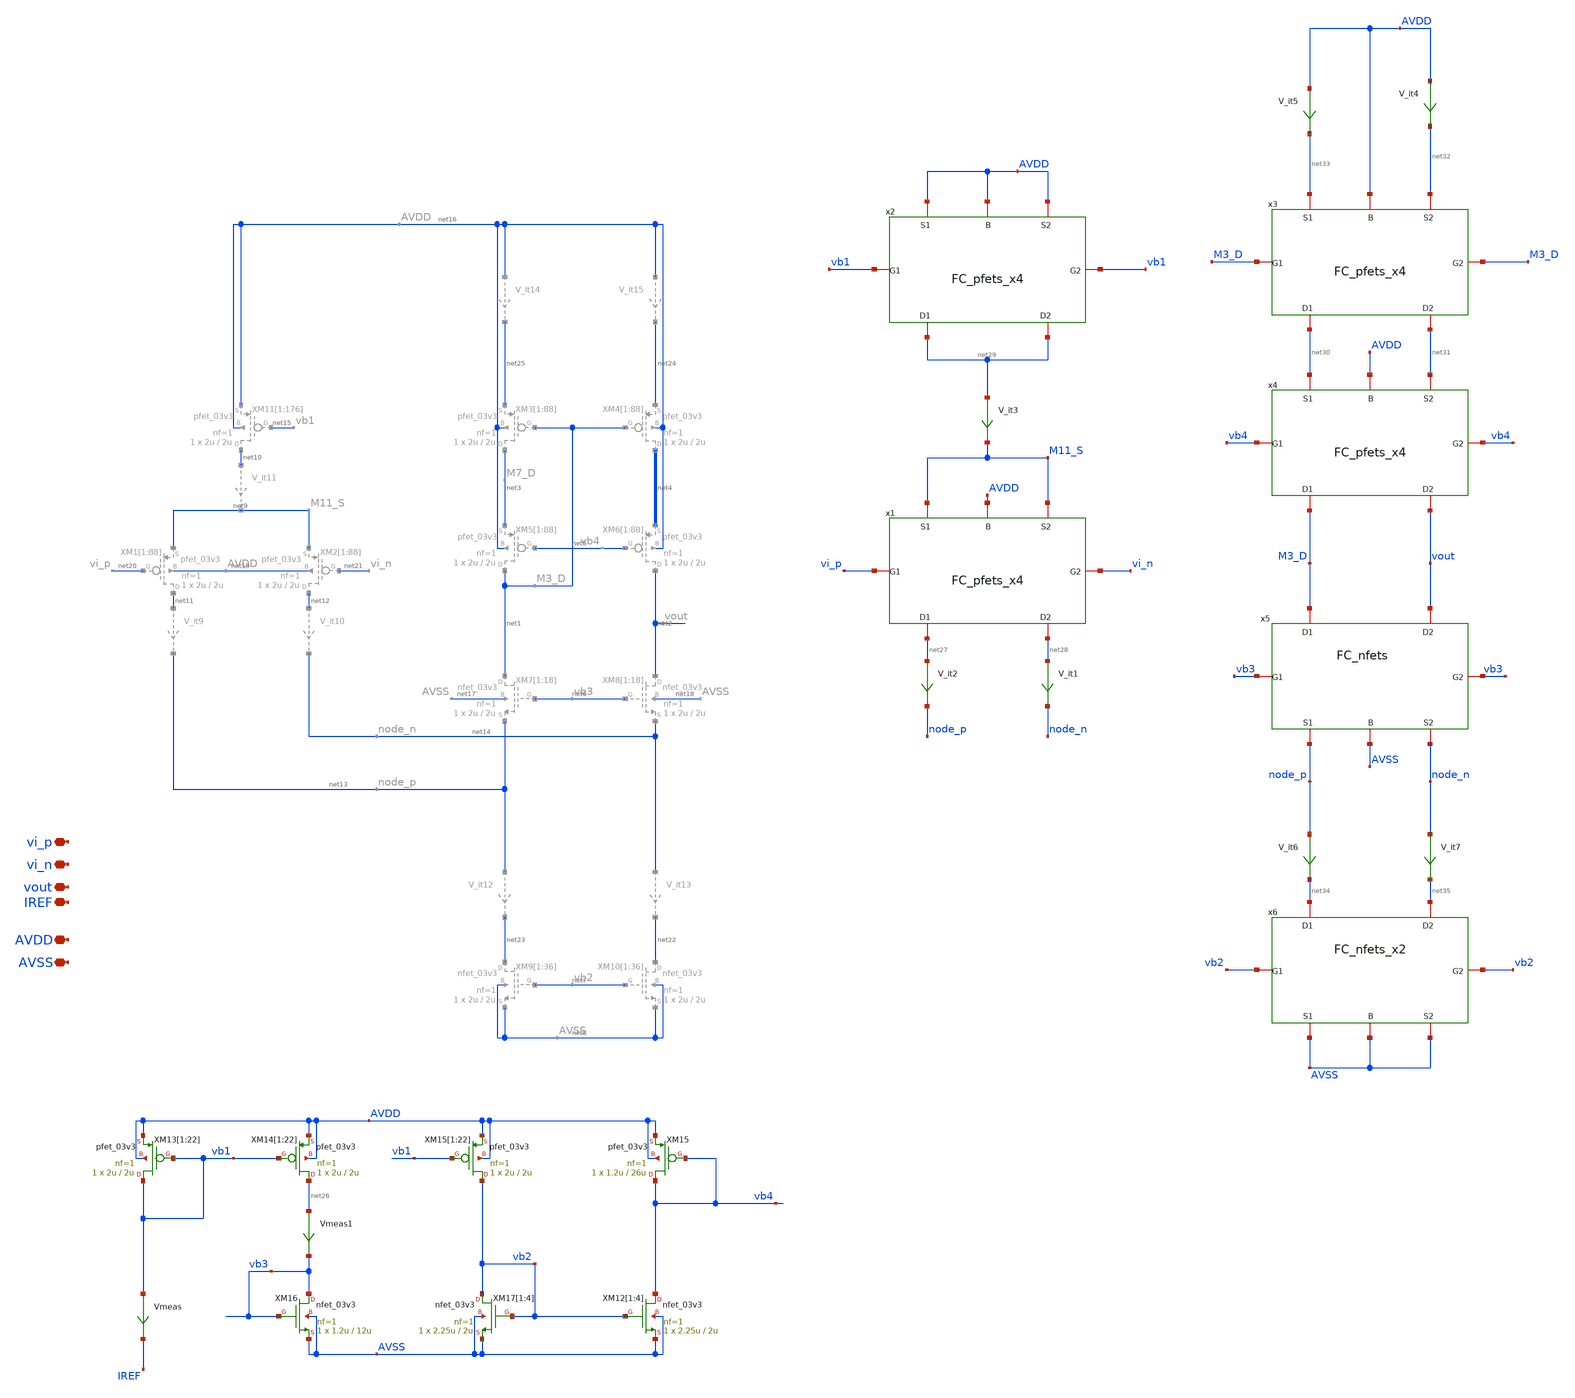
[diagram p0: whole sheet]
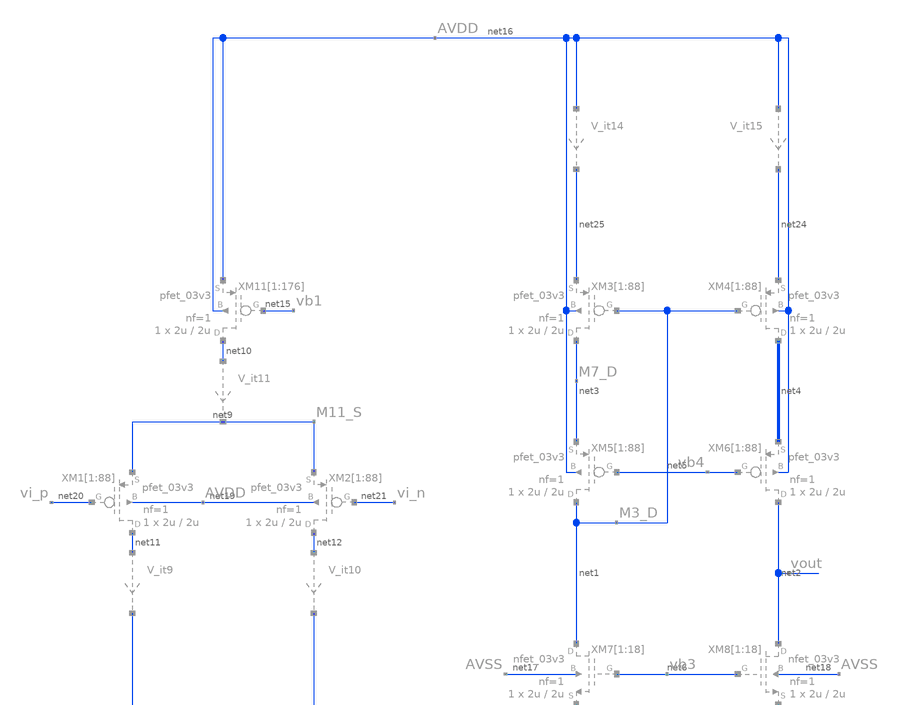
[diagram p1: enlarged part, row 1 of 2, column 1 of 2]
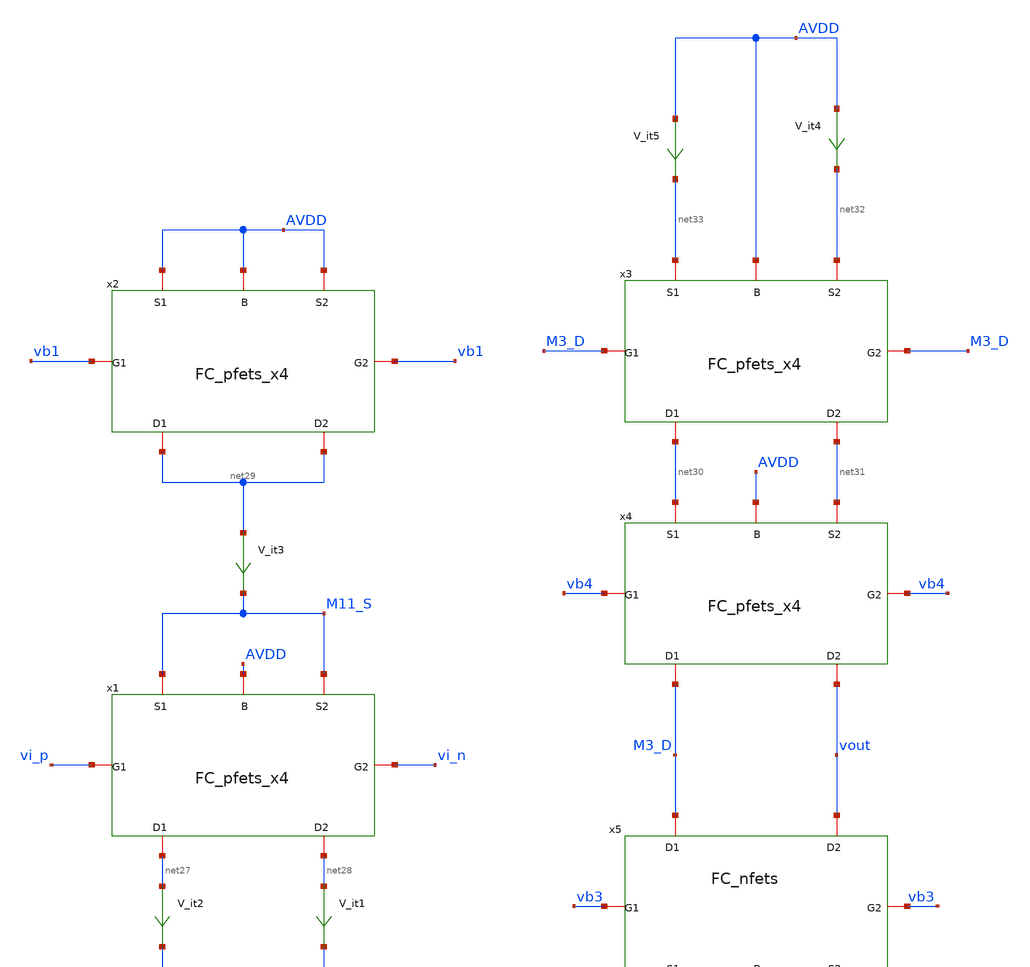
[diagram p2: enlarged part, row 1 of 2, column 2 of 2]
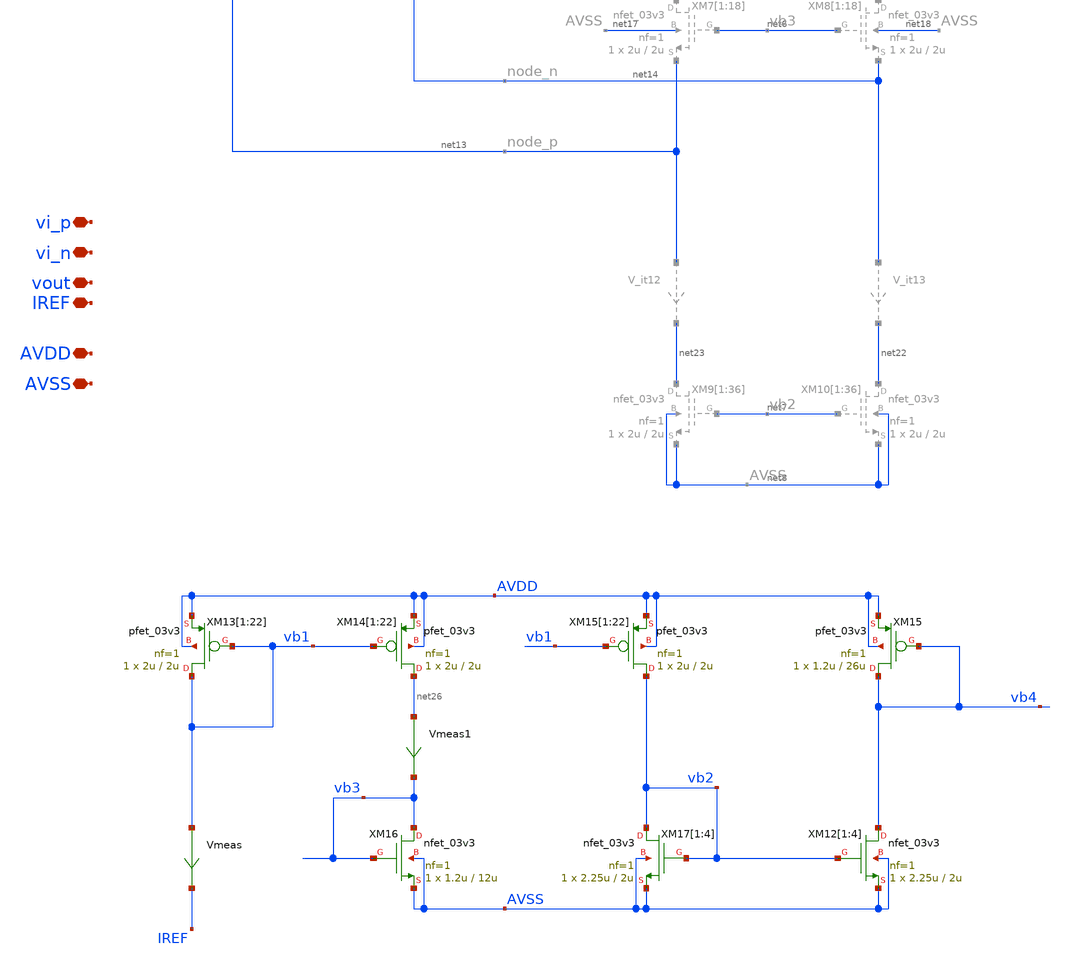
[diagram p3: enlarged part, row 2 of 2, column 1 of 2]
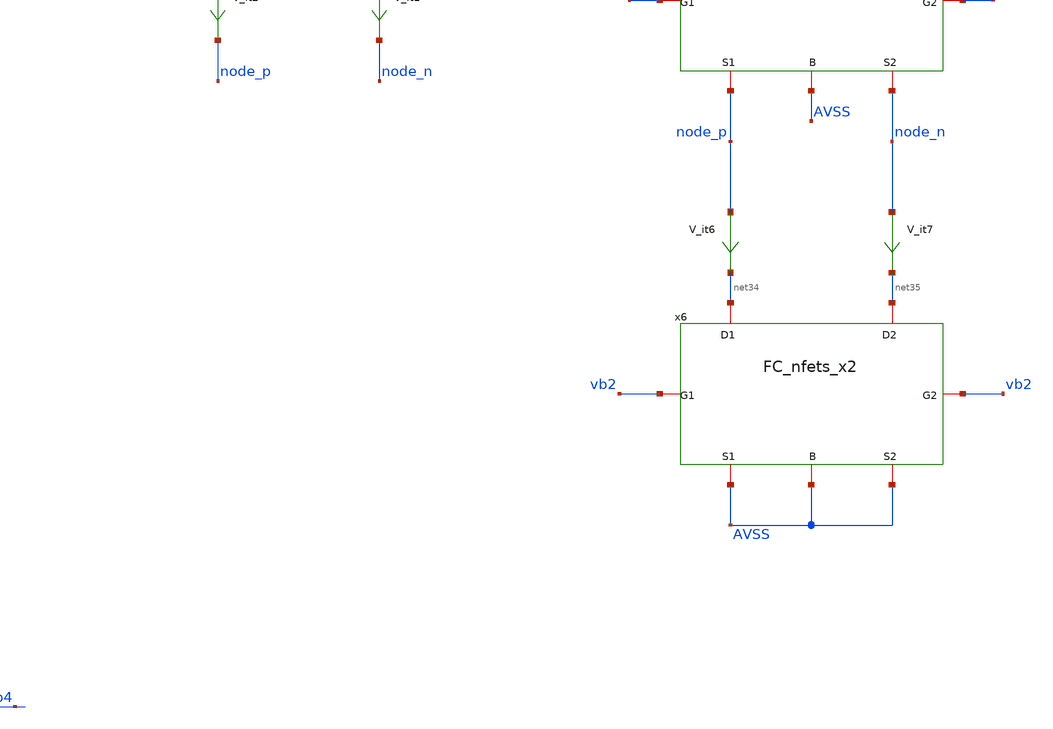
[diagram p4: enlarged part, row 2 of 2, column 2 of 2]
** sch_path: TIA_Filter/Folded/FoldedCascode.sch
**.subckt FoldedCascode AVDD AVSS vout vi_p vi_n IREF
*.iopin AVDD
*.iopin AVSS
*.iopin vout
*.iopin vi_p
*.iopin vi_n
*.iopin IREF
XM16 vb3 vb3 AVSS AVSS nfet_03v3 L=12u W=1.2u nf=1 ad='int((nf+1)/2) * W/nf * 0.18u' as='int((nf+2)/2) * W/nf * 0.18u'
+ pd='2*int((nf+1)/2) * (W/nf + 0.18u)' ps='2*int((nf+2)/2) * (W/nf + 0.18u)' nrd='0.18u / W' nrs='0.18u / W'
+ sa=0 sb=0 sd=0 m=1
XM13[1] vb1 vb1 AVDD AVDD pfet_03v3 L=2u W=2u nf=1 ad='int((nf+1)/2) * W/nf * 0.18u' as='int((nf+2)/2) * W/nf * 0.18u'
+ pd='2*int((nf+1)/2) * (W/nf + 0.18u)' ps='2*int((nf+2)/2) * (W/nf + 0.18u)' nrd='0.18u / W' nrs='0.18u / W'
+ sa=0 sb=0 sd=0 m=1
XM13[2] vb1 vb1 AVDD AVDD pfet_03v3 L=2u W=2u nf=1 ad='int((nf+1)/2) * W/nf * 0.18u' as='int((nf+2)/2) * W/nf * 0.18u'
+ pd='2*int((nf+1)/2) * (W/nf + 0.18u)' ps='2*int((nf+2)/2) * (W/nf + 0.18u)' nrd='0.18u / W' nrs='0.18u / W'
+ sa=0 sb=0 sd=0 m=1
XM13[3] vb1 vb1 AVDD AVDD pfet_03v3 L=2u W=2u nf=1 ad='int((nf+1)/2) * W/nf * 0.18u' as='int((nf+2)/2) * W/nf * 0.18u'
+ pd='2*int((nf+1)/2) * (W/nf + 0.18u)' ps='2*int((nf+2)/2) * (W/nf + 0.18u)' nrd='0.18u / W' nrs='0.18u / W'
+ sa=0 sb=0 sd=0 m=1
XM13[4] vb1 vb1 AVDD AVDD pfet_03v3 L=2u W=2u nf=1 ad='int((nf+1)/2) * W/nf * 0.18u' as='int((nf+2)/2) * W/nf * 0.18u'
+ pd='2*int((nf+1)/2) * (W/nf + 0.18u)' ps='2*int((nf+2)/2) * (W/nf + 0.18u)' nrd='0.18u / W' nrs='0.18u / W'
+ sa=0 sb=0 sd=0 m=1
XM13[5] vb1 vb1 AVDD AVDD pfet_03v3 L=2u W=2u nf=1 ad='int((nf+1)/2) * W/nf * 0.18u' as='int((nf+2)/2) * W/nf * 0.18u'
+ pd='2*int((nf+1)/2) * (W/nf + 0.18u)' ps='2*int((nf+2)/2) * (W/nf + 0.18u)' nrd='0.18u / W' nrs='0.18u / W'
+ sa=0 sb=0 sd=0 m=1
XM13[6] vb1 vb1 AVDD AVDD pfet_03v3 L=2u W=2u nf=1 ad='int((nf+1)/2) * W/nf * 0.18u' as='int((nf+2)/2) * W/nf * 0.18u'
+ pd='2*int((nf+1)/2) * (W/nf + 0.18u)' ps='2*int((nf+2)/2) * (W/nf + 0.18u)' nrd='0.18u / W' nrs='0.18u / W'
+ sa=0 sb=0 sd=0 m=1
XM13[7] vb1 vb1 AVDD AVDD pfet_03v3 L=2u W=2u nf=1 ad='int((nf+1)/2) * W/nf * 0.18u' as='int((nf+2)/2) * W/nf * 0.18u'
+ pd='2*int((nf+1)/2) * (W/nf + 0.18u)' ps='2*int((nf+2)/2) * (W/nf + 0.18u)' nrd='0.18u / W' nrs='0.18u / W'
+ sa=0 sb=0 sd=0 m=1
XM13[8] vb1 vb1 AVDD AVDD pfet_03v3 L=2u W=2u nf=1 ad='int((nf+1)/2) * W/nf * 0.18u' as='int((nf+2)/2) * W/nf * 0.18u'
+ pd='2*int((nf+1)/2) * (W/nf + 0.18u)' ps='2*int((nf+2)/2) * (W/nf + 0.18u)' nrd='0.18u / W' nrs='0.18u / W'
+ sa=0 sb=0 sd=0 m=1
XM13[9] vb1 vb1 AVDD AVDD pfet_03v3 L=2u W=2u nf=1 ad='int((nf+1)/2) * W/nf * 0.18u' as='int((nf+2)/2) * W/nf * 0.18u'
+ pd='2*int((nf+1)/2) * (W/nf + 0.18u)' ps='2*int((nf+2)/2) * (W/nf + 0.18u)' nrd='0.18u / W' nrs='0.18u / W'
+ sa=0 sb=0 sd=0 m=1
XM13[10] vb1 vb1 AVDD AVDD pfet_03v3 L=2u W=2u nf=1 ad='int((nf+1)/2) * W/nf * 0.18u' as='int((nf+2)/2) * W/nf * 0.18u'
+ pd='2*int((nf+1)/2) * (W/nf + 0.18u)' ps='2*int((nf+2)/2) * (W/nf + 0.18u)' nrd='0.18u / W' nrs='0.18u / W'
+ sa=0 sb=0 sd=0 m=1
XM13[11] vb1 vb1 AVDD AVDD pfet_03v3 L=2u W=2u nf=1 ad='int((nf+1)/2) * W/nf * 0.18u' as='int((nf+2)/2) * W/nf * 0.18u'
+ pd='2*int((nf+1)/2) * (W/nf + 0.18u)' ps='2*int((nf+2)/2) * (W/nf + 0.18u)' nrd='0.18u / W' nrs='0.18u / W'
+ sa=0 sb=0 sd=0 m=1
XM13[12] vb1 vb1 AVDD AVDD pfet_03v3 L=2u W=2u nf=1 ad='int((nf+1)/2) * W/nf * 0.18u' as='int((nf+2)/2) * W/nf * 0.18u'
+ pd='2*int((nf+1)/2) * (W/nf + 0.18u)' ps='2*int((nf+2)/2) * (W/nf + 0.18u)' nrd='0.18u / W' nrs='0.18u / W'
+ sa=0 sb=0 sd=0 m=1
XM13[13] vb1 vb1 AVDD AVDD pfet_03v3 L=2u W=2u nf=1 ad='int((nf+1)/2) * W/nf * 0.18u' as='int((nf+2)/2) * W/nf * 0.18u'
+ pd='2*int((nf+1)/2) * (W/nf + 0.18u)' ps='2*int((nf+2)/2) * (W/nf + 0.18u)' nrd='0.18u / W' nrs='0.18u / W'
+ sa=0 sb=0 sd=0 m=1
XM13[14] vb1 vb1 AVDD AVDD pfet_03v3 L=2u W=2u nf=1 ad='int((nf+1)/2) * W/nf * 0.18u' as='int((nf+2)/2) * W/nf * 0.18u'
+ pd='2*int((nf+1)/2) * (W/nf + 0.18u)' ps='2*int((nf+2)/2) * (W/nf + 0.18u)' nrd='0.18u / W' nrs='0.18u / W'
+ sa=0 sb=0 sd=0 m=1
XM13[15] vb1 vb1 AVDD AVDD pfet_03v3 L=2u W=2u nf=1 ad='int((nf+1)/2) * W/nf * 0.18u' as='int((nf+2)/2) * W/nf * 0.18u'
+ pd='2*int((nf+1)/2) * (W/nf + 0.18u)' ps='2*int((nf+2)/2) * (W/nf + 0.18u)' nrd='0.18u / W' nrs='0.18u / W'
+ sa=0 sb=0 sd=0 m=1
XM13[16] vb1 vb1 AVDD AVDD pfet_03v3 L=2u W=2u nf=1 ad='int((nf+1)/2) * W/nf * 0.18u' as='int((nf+2)/2) * W/nf * 0.18u'
+ pd='2*int((nf+1)/2) * (W/nf + 0.18u)' ps='2*int((nf+2)/2) * (W/nf + 0.18u)' nrd='0.18u / W' nrs='0.18u / W'
+ sa=0 sb=0 sd=0 m=1
XM13[17] vb1 vb1 AVDD AVDD pfet_03v3 L=2u W=2u nf=1 ad='int((nf+1)/2) * W/nf * 0.18u' as='int((nf+2)/2) * W/nf * 0.18u'
+ pd='2*int((nf+1)/2) * (W/nf + 0.18u)' ps='2*int((nf+2)/2) * (W/nf + 0.18u)' nrd='0.18u / W' nrs='0.18u / W'
+ sa=0 sb=0 sd=0 m=1
XM13[18] vb1 vb1 AVDD AVDD pfet_03v3 L=2u W=2u nf=1 ad='int((nf+1)/2) * W/nf * 0.18u' as='int((nf+2)/2) * W/nf * 0.18u'
+ pd='2*int((nf+1)/2) * (W/nf + 0.18u)' ps='2*int((nf+2)/2) * (W/nf + 0.18u)' nrd='0.18u / W' nrs='0.18u / W'
+ sa=0 sb=0 sd=0 m=1
XM13[19] vb1 vb1 AVDD AVDD pfet_03v3 L=2u W=2u nf=1 ad='int((nf+1)/2) * W/nf * 0.18u' as='int((nf+2)/2) * W/nf * 0.18u'
+ pd='2*int((nf+1)/2) * (W/nf + 0.18u)' ps='2*int((nf+2)/2) * (W/nf + 0.18u)' nrd='0.18u / W' nrs='0.18u / W'
+ sa=0 sb=0 sd=0 m=1
XM13[20] vb1 vb1 AVDD AVDD pfet_03v3 L=2u W=2u nf=1 ad='int((nf+1)/2) * W/nf * 0.18u' as='int((nf+2)/2) * W/nf * 0.18u'
+ pd='2*int((nf+1)/2) * (W/nf + 0.18u)' ps='2*int((nf+2)/2) * (W/nf + 0.18u)' nrd='0.18u / W' nrs='0.18u / W'
+ sa=0 sb=0 sd=0 m=1
XM13[21] vb1 vb1 AVDD AVDD pfet_03v3 L=2u W=2u nf=1 ad='int((nf+1)/2) * W/nf * 0.18u' as='int((nf+2)/2) * W/nf * 0.18u'
+ pd='2*int((nf+1)/2) * (W/nf + 0.18u)' ps='2*int((nf+2)/2) * (W/nf + 0.18u)' nrd='0.18u / W' nrs='0.18u / W'
+ sa=0 sb=0 sd=0 m=1
XM13[22] vb1 vb1 AVDD AVDD pfet_03v3 L=2u W=2u nf=1 ad='int((nf+1)/2) * W/nf * 0.18u' as='int((nf+2)/2) * W/nf * 0.18u'
+ pd='2*int((nf+1)/2) * (W/nf + 0.18u)' ps='2*int((nf+2)/2) * (W/nf + 0.18u)' nrd='0.18u / W' nrs='0.18u / W'
+ sa=0 sb=0 sd=0 m=1
XM14[1] net26 vb1 AVDD AVDD pfet_03v3 L=2u W=2u nf=1 ad='int((nf+1)/2) * W/nf * 0.18u' as='int((nf+2)/2) * W/nf * 0.18u'
+ pd='2*int((nf+1)/2) * (W/nf + 0.18u)' ps='2*int((nf+2)/2) * (W/nf + 0.18u)' nrd='0.18u / W' nrs='0.18u / W'
+ sa=0 sb=0 sd=0 m=1
XM14[2] net26 vb1 AVDD AVDD pfet_03v3 L=2u W=2u nf=1 ad='int((nf+1)/2) * W/nf * 0.18u' as='int((nf+2)/2) * W/nf * 0.18u'
+ pd='2*int((nf+1)/2) * (W/nf + 0.18u)' ps='2*int((nf+2)/2) * (W/nf + 0.18u)' nrd='0.18u / W' nrs='0.18u / W'
+ sa=0 sb=0 sd=0 m=1
XM14[3] net26 vb1 AVDD AVDD pfet_03v3 L=2u W=2u nf=1 ad='int((nf+1)/2) * W/nf * 0.18u' as='int((nf+2)/2) * W/nf * 0.18u'
+ pd='2*int((nf+1)/2) * (W/nf + 0.18u)' ps='2*int((nf+2)/2) * (W/nf + 0.18u)' nrd='0.18u / W' nrs='0.18u / W'
+ sa=0 sb=0 sd=0 m=1
XM14[4] net26 vb1 AVDD AVDD pfet_03v3 L=2u W=2u nf=1 ad='int((nf+1)/2) * W/nf * 0.18u' as='int((nf+2)/2) * W/nf * 0.18u'
+ pd='2*int((nf+1)/2) * (W/nf + 0.18u)' ps='2*int((nf+2)/2) * (W/nf + 0.18u)' nrd='0.18u / W' nrs='0.18u / W'
+ sa=0 sb=0 sd=0 m=1
XM14[5] net26 vb1 AVDD AVDD pfet_03v3 L=2u W=2u nf=1 ad='int((nf+1)/2) * W/nf * 0.18u' as='int((nf+2)/2) * W/nf * 0.18u'
+ pd='2*int((nf+1)/2) * (W/nf + 0.18u)' ps='2*int((nf+2)/2) * (W/nf + 0.18u)' nrd='0.18u / W' nrs='0.18u / W'
+ sa=0 sb=0 sd=0 m=1
XM14[6] net26 vb1 AVDD AVDD pfet_03v3 L=2u W=2u nf=1 ad='int((nf+1)/2) * W/nf * 0.18u' as='int((nf+2)/2) * W/nf * 0.18u'
+ pd='2*int((nf+1)/2) * (W/nf + 0.18u)' ps='2*int((nf+2)/2) * (W/nf + 0.18u)' nrd='0.18u / W' nrs='0.18u / W'
+ sa=0 sb=0 sd=0 m=1
XM14[7] net26 vb1 AVDD AVDD pfet_03v3 L=2u W=2u nf=1 ad='int((nf+1)/2) * W/nf * 0.18u' as='int((nf+2)/2) * W/nf * 0.18u'
+ pd='2*int((nf+1)/2) * (W/nf + 0.18u)' ps='2*int((nf+2)/2) * (W/nf + 0.18u)' nrd='0.18u / W' nrs='0.18u / W'
+ sa=0 sb=0 sd=0 m=1
XM14[8] net26 vb1 AVDD AVDD pfet_03v3 L=2u W=2u nf=1 ad='int((nf+1)/2) * W/nf * 0.18u' as='int((nf+2)/2) * W/nf * 0.18u'
+ pd='2*int((nf+1)/2) * (W/nf + 0.18u)' ps='2*int((nf+2)/2) * (W/nf + 0.18u)' nrd='0.18u / W' nrs='0.18u / W'
+ sa=0 sb=0 sd=0 m=1
XM14[9] net26 vb1 AVDD AVDD pfet_03v3 L=2u W=2u nf=1 ad='int((nf+1)/2) * W/nf * 0.18u' as='int((nf+2)/2) * W/nf * 0.18u'
+ pd='2*int((nf+1)/2) * (W/nf + 0.18u)' ps='2*int((nf+2)/2) * (W/nf + 0.18u)' nrd='0.18u / W' nrs='0.18u / W'
+ sa=0 sb=0 sd=0 m=1
XM14[10] net26 vb1 AVDD AVDD pfet_03v3 L=2u W=2u nf=1 ad='int((nf+1)/2) * W/nf * 0.18u' as='int((nf+2)/2) * W/nf * 0.18u'
+ pd='2*int((nf+1)/2) * (W/nf + 0.18u)' ps='2*int((nf+2)/2) * (W/nf + 0.18u)' nrd='0.18u / W' nrs='0.18u / W'
+ sa=0 sb=0 sd=0 m=1
XM14[11] net26 vb1 AVDD AVDD pfet_03v3 L=2u W=2u nf=1 ad='int((nf+1)/2) * W/nf * 0.18u' as='int((nf+2)/2) * W/nf * 0.18u'
+ pd='2*int((nf+1)/2) * (W/nf + 0.18u)' ps='2*int((nf+2)/2) * (W/nf + 0.18u)' nrd='0.18u / W' nrs='0.18u / W'
+ sa=0 sb=0 sd=0 m=1
XM14[12] net26 vb1 AVDD AVDD pfet_03v3 L=2u W=2u nf=1 ad='int((nf+1)/2) * W/nf * 0.18u' as='int((nf+2)/2) * W/nf * 0.18u'
+ pd='2*int((nf+1)/2) * (W/nf + 0.18u)' ps='2*int((nf+2)/2) * (W/nf + 0.18u)' nrd='0.18u / W' nrs='0.18u / W'
+ sa=0 sb=0 sd=0 m=1
XM14[13] net26 vb1 AVDD AVDD pfet_03v3 L=2u W=2u nf=1 ad='int((nf+1)/2) * W/nf * 0.18u' as='int((nf+2)/2) * W/nf * 0.18u'
+ pd='2*int((nf+1)/2) * (W/nf + 0.18u)' ps='2*int((nf+2)/2) * (W/nf + 0.18u)' nrd='0.18u / W' nrs='0.18u / W'
+ sa=0 sb=0 sd=0 m=1
XM14[14] net26 vb1 AVDD AVDD pfet_03v3 L=2u W=2u nf=1 ad='int((nf+1)/2) * W/nf * 0.18u' as='int((nf+2)/2) * W/nf * 0.18u'
+ pd='2*int((nf+1)/2) * (W/nf + 0.18u)' ps='2*int((nf+2)/2) * (W/nf + 0.18u)' nrd='0.18u / W' nrs='0.18u / W'
+ sa=0 sb=0 sd=0 m=1
XM14[15] net26 vb1 AVDD AVDD pfet_03v3 L=2u W=2u nf=1 ad='int((nf+1)/2) * W/nf * 0.18u' as='int((nf+2)/2) * W/nf * 0.18u'
+ pd='2*int((nf+1)/2) * (W/nf + 0.18u)' ps='2*int((nf+2)/2) * (W/nf + 0.18u)' nrd='0.18u / W' nrs='0.18u / W'
+ sa=0 sb=0 sd=0 m=1
XM14[16] net26 vb1 AVDD AVDD pfet_03v3 L=2u W=2u nf=1 ad='int((nf+1)/2) * W/nf * 0.18u' as='int((nf+2)/2) * W/nf * 0.18u'
+ pd='2*int((nf+1)/2) * (W/nf + 0.18u)' ps='2*int((nf+2)/2) * (W/nf + 0.18u)' nrd='0.18u / W' nrs='0.18u / W'
+ sa=0 sb=0 sd=0 m=1
XM14[17] net26 vb1 AVDD AVDD pfet_03v3 L=2u W=2u nf=1 ad='int((nf+1)/2) * W/nf * 0.18u' as='int((nf+2)/2) * W/nf * 0.18u'
+ pd='2*int((nf+1)/2) * (W/nf + 0.18u)' ps='2*int((nf+2)/2) * (W/nf + 0.18u)' nrd='0.18u / W' nrs='0.18u / W'
+ sa=0 sb=0 sd=0 m=1
XM14[18] net26 vb1 AVDD AVDD pfet_03v3 L=2u W=2u nf=1 ad='int((nf+1)/2) * W/nf * 0.18u' as='int((nf+2)/2) * W/nf * 0.18u'
+ pd='2*int((nf+1)/2) * (W/nf + 0.18u)' ps='2*int((nf+2)/2) * (W/nf + 0.18u)' nrd='0.18u / W' nrs='0.18u / W'
+ sa=0 sb=0 sd=0 m=1
XM14[19] net26 vb1 AVDD AVDD pfet_03v3 L=2u W=2u nf=1 ad='int((nf+1)/2) * W/nf * 0.18u' as='int((nf+2)/2) * W/nf * 0.18u'
+ pd='2*int((nf+1)/2) * (W/nf + 0.18u)' ps='2*int((nf+2)/2) * (W/nf + 0.18u)' nrd='0.18u / W' nrs='0.18u / W'
+ sa=0 sb=0 sd=0 m=1
XM14[20] net26 vb1 AVDD AVDD pfet_03v3 L=2u W=2u nf=1 ad='int((nf+1)/2) * W/nf * 0.18u' as='int((nf+2)/2) * W/nf * 0.18u'
+ pd='2*int((nf+1)/2) * (W/nf + 0.18u)' ps='2*int((nf+2)/2) * (W/nf + 0.18u)' nrd='0.18u / W' nrs='0.18u / W'
+ sa=0 sb=0 sd=0 m=1
XM14[21] net26 vb1 AVDD AVDD pfet_03v3 L=2u W=2u nf=1 ad='int((nf+1)/2) * W/nf * 0.18u' as='int((nf+2)/2) * W/nf * 0.18u'
+ pd='2*int((nf+1)/2) * (W/nf + 0.18u)' ps='2*int((nf+2)/2) * (W/nf + 0.18u)' nrd='0.18u / W' nrs='0.18u / W'
+ sa=0 sb=0 sd=0 m=1
XM14[22] net26 vb1 AVDD AVDD pfet_03v3 L=2u W=2u nf=1 ad='int((nf+1)/2) * W/nf * 0.18u' as='int((nf+2)/2) * W/nf * 0.18u'
+ pd='2*int((nf+1)/2) * (W/nf + 0.18u)' ps='2*int((nf+2)/2) * (W/nf + 0.18u)' nrd='0.18u / W' nrs='0.18u / W'
+ sa=0 sb=0 sd=0 m=1
XM15[1] vb2 vb1 AVDD AVDD pfet_03v3 L=2u W=2u nf=1 ad='int((nf+1)/2) * W/nf * 0.18u' as='int((nf+2)/2) * W/nf * 0.18u'
+ pd='2*int((nf+1)/2) * (W/nf + 0.18u)' ps='2*int((nf+2)/2) * (W/nf + 0.18u)' nrd='0.18u / W' nrs='0.18u / W'
+ sa=0 sb=0 sd=0 m=1
XM15[2] vb2 vb1 AVDD AVDD pfet_03v3 L=2u W=2u nf=1 ad='int((nf+1)/2) * W/nf * 0.18u' as='int((nf+2)/2) * W/nf * 0.18u'
+ pd='2*int((nf+1)/2) * (W/nf + 0.18u)' ps='2*int((nf+2)/2) * (W/nf + 0.18u)' nrd='0.18u / W' nrs='0.18u / W'
+ sa=0 sb=0 sd=0 m=1
XM15[3] vb2 vb1 AVDD AVDD pfet_03v3 L=2u W=2u nf=1 ad='int((nf+1)/2) * W/nf * 0.18u' as='int((nf+2)/2) * W/nf * 0.18u'
+ pd='2*int((nf+1)/2) * (W/nf + 0.18u)' ps='2*int((nf+2)/2) * (W/nf + 0.18u)' nrd='0.18u / W' nrs='0.18u / W'
+ sa=0 sb=0 sd=0 m=1
XM15[4] vb2 vb1 AVDD AVDD pfet_03v3 L=2u W=2u nf=1 ad='int((nf+1)/2) * W/nf * 0.18u' as='int((nf+2)/2) * W/nf * 0.18u'
+ pd='2*int((nf+1)/2) * (W/nf + 0.18u)' ps='2*int((nf+2)/2) * (W/nf + 0.18u)' nrd='0.18u / W' nrs='0.18u / W'
+ sa=0 sb=0 sd=0 m=1
XM15[5] vb2 vb1 AVDD AVDD pfet_03v3 L=2u W=2u nf=1 ad='int((nf+1)/2) * W/nf * 0.18u' as='int((nf+2)/2) * W/nf * 0.18u'
+ pd='2*int((nf+1)/2) * (W/nf + 0.18u)' ps='2*int((nf+2)/2) * (W/nf + 0.18u)' nrd='0.18u / W' nrs='0.18u / W'
+ sa=0 sb=0 sd=0 m=1
XM15[6] vb2 vb1 AVDD AVDD pfet_03v3 L=2u W=2u nf=1 ad='int((nf+1)/2) * W/nf * 0.18u' as='int((nf+2)/2) * W/nf * 0.18u'
+ pd='2*int((nf+1)/2) * (W/nf + 0.18u)' ps='2*int((nf+2)/2) * (W/nf + 0.18u)' nrd='0.18u / W' nrs='0.18u / W'
+ sa=0 sb=0 sd=0 m=1
XM15[7] vb2 vb1 AVDD AVDD pfet_03v3 L=2u W=2u nf=1 ad='int((nf+1)/2) * W/nf * 0.18u' as='int((nf+2)/2) * W/nf * 0.18u'
+ pd='2*int((nf+1)/2) * (W/nf + 0.18u)' ps='2*int((nf+2)/2) * (W/nf + 0.18u)' nrd='0.18u / W' nrs='0.18u / W'
+ sa=0 sb=0 sd=0 m=1
XM15[8] vb2 vb1 AVDD AVDD pfet_03v3 L=2u W=2u nf=1 ad='int((nf+1)/2) * W/nf * 0.18u' as='int((nf+2)/2) * W/nf * 0.18u'
+ pd='2*int((nf+1)/2) * (W/nf + 0.18u)' ps='2*int((nf+2)/2) * (W/nf + 0.18u)' nrd='0.18u / W' nrs='0.18u / W'
+ sa=0 sb=0 sd=0 m=1
XM15[9] vb2 vb1 AVDD AVDD pfet_03v3 L=2u W=2u nf=1 ad='int((nf+1)/2) * W/nf * 0.18u' as='int((nf+2)/2) * W/nf * 0.18u'
+ pd='2*int((nf+1)/2) * (W/nf + 0.18u)' ps='2*int((nf+2)/2) * (W/nf + 0.18u)' nrd='0.18u / W' nrs='0.18u / W'
+ sa=0 sb=0 sd=0 m=1
XM15[10] vb2 vb1 AVDD AVDD pfet_03v3 L=2u W=2u nf=1 ad='int((nf+1)/2) * W/nf * 0.18u' as='int((nf+2)/2) * W/nf * 0.18u'
+ pd='2*int((nf+1)/2) * (W/nf + 0.18u)' ps='2*int((nf+2)/2) * (W/nf + 0.18u)' nrd='0.18u / W' nrs='0.18u / W'
+ sa=0 sb=0 sd=0 m=1
XM15[11] vb2 vb1 AVDD AVDD pfet_03v3 L=2u W=2u nf=1 ad='int((nf+1)/2) * W/nf * 0.18u' as='int((nf+2)/2) * W/nf * 0.18u'
+ pd='2*int((nf+1)/2) * (W/nf + 0.18u)' ps='2*int((nf+2)/2) * (W/nf + 0.18u)' nrd='0.18u / W' nrs='0.18u / W'
+ sa=0 sb=0 sd=0 m=1
XM15[12] vb2 vb1 AVDD AVDD pfet_03v3 L=2u W=2u nf=1 ad='int((nf+1)/2) * W/nf * 0.18u' as='int((nf+2)/2) * W/nf * 0.18u'
+ pd='2*int((nf+1)/2) * (W/nf + 0.18u)' ps='2*int((nf+2)/2) * (W/nf + 0.18u)' nrd='0.18u / W' nrs='0.18u / W'
+ sa=0 sb=0 sd=0 m=1
XM15[13] vb2 vb1 AVDD AVDD pfet_03v3 L=2u W=2u nf=1 ad='int((nf+1)/2) * W/nf * 0.18u' as='int((nf+2)/2) * W/nf * 0.18u'
+ pd='2*int((nf+1)/2) * (W/nf + 0.18u)' ps='2*int((nf+2)/2) * (W/nf + 0.18u)' nrd='0.18u / W' nrs='0.18u / W'
+ sa=0 sb=0 sd=0 m=1
XM15[14] vb2 vb1 AVDD AVDD pfet_03v3 L=2u W=2u nf=1 ad='int((nf+1)/2) * W/nf * 0.18u' as='int((nf+2)/2) * W/nf * 0.18u'
+ pd='2*int((nf+1)/2) * (W/nf + 0.18u)' ps='2*int((nf+2)/2) * (W/nf + 0.18u)' nrd='0.18u / W' nrs='0.18u / W'
+ sa=0 sb=0 sd=0 m=1
XM15[15] vb2 vb1 AVDD AVDD pfet_03v3 L=2u W=2u nf=1 ad='int((nf+1)/2) * W/nf * 0.18u' as='int((nf+2)/2) * W/nf * 0.18u'
+ pd='2*int((nf+1)/2) * (W/nf + 0.18u)' ps='2*int((nf+2)/2) * (W/nf + 0.18u)' nrd='0.18u / W' nrs='0.18u / W'
+ sa=0 sb=0 sd=0 m=1
XM15[16] vb2 vb1 AVDD AVDD pfet_03v3 L=2u W=2u nf=1 ad='int((nf+1)/2) * W/nf * 0.18u' as='int((nf+2)/2) * W/nf * 0.18u'
+ pd='2*int((nf+1)/2) * (W/nf + 0.18u)' ps='2*int((nf+2)/2) * (W/nf + 0.18u)' nrd='0.18u / W' nrs='0.18u / W'
+ sa=0 sb=0 sd=0 m=1
XM15[17] vb2 vb1 AVDD AVDD pfet_03v3 L=2u W=2u nf=1 ad='int((nf+1)/2) * W/nf * 0.18u' as='int((nf+2)/2) * W/nf * 0.18u'
+ pd='2*int((nf+1)/2) * (W/nf + 0.18u)' ps='2*int((nf+2)/2) * (W/nf + 0.18u)' nrd='0.18u / W' nrs='0.18u / W'
+ sa=0 sb=0 sd=0 m=1
XM15[18] vb2 vb1 AVDD AVDD pfet_03v3 L=2u W=2u nf=1 ad='int((nf+1)/2) * W/nf * 0.18u' as='int((nf+2)/2) * W/nf * 0.18u'
+ pd='2*int((nf+1)/2) * (W/nf + 0.18u)' ps='2*int((nf+2)/2) * (W/nf + 0.18u)' nrd='0.18u / W' nrs='0.18u / W'
+ sa=0 sb=0 sd=0 m=1
XM15[19] vb2 vb1 AVDD AVDD pfet_03v3 L=2u W=2u nf=1 ad='int((nf+1)/2) * W/nf * 0.18u' as='int((nf+2)/2) * W/nf * 0.18u'
+ pd='2*int((nf+1)/2) * (W/nf + 0.18u)' ps='2*int((nf+2)/2) * (W/nf + 0.18u)' nrd='0.18u / W' nrs='0.18u / W'
+ sa=0 sb=0 sd=0 m=1
XM15[20] vb2 vb1 AVDD AVDD pfet_03v3 L=2u W=2u nf=1 ad='int((nf+1)/2) * W/nf * 0.18u' as='int((nf+2)/2) * W/nf * 0.18u'
+ pd='2*int((nf+1)/2) * (W/nf + 0.18u)' ps='2*int((nf+2)/2) * (W/nf + 0.18u)' nrd='0.18u / W' nrs='0.18u / W'
+ sa=0 sb=0 sd=0 m=1
XM15[21] vb2 vb1 AVDD AVDD pfet_03v3 L=2u W=2u nf=1 ad='int((nf+1)/2) * W/nf * 0.18u' as='int((nf+2)/2) * W/nf * 0.18u'
+ pd='2*int((nf+1)/2) * (W/nf + 0.18u)' ps='2*int((nf+2)/2) * (W/nf + 0.18u)' nrd='0.18u / W' nrs='0.18u / W'
+ sa=0 sb=0 sd=0 m=1
XM15[22] vb2 vb1 AVDD AVDD pfet_03v3 L=2u W=2u nf=1 ad='int((nf+1)/2) * W/nf * 0.18u' as='int((nf+2)/2) * W/nf * 0.18u'
+ pd='2*int((nf+1)/2) * (W/nf + 0.18u)' ps='2*int((nf+2)/2) * (W/nf + 0.18u)' nrd='0.18u / W' nrs='0.18u / W'
+ sa=0 sb=0 sd=0 m=1
XM15 vb4 vb4 AVDD AVDD pfet_03v3 L=26u W=1.2u nf=1 ad='int((nf+1)/2) * W/nf * 0.18u' as='int((nf+2)/2) * W/nf * 0.18u'
+ pd='2*int((nf+1)/2) * (W/nf + 0.18u)' ps='2*int((nf+2)/2) * (W/nf + 0.18u)' nrd='0.18u / W' nrs='0.18u / W'
+ sa=0 sb=0 sd=0 m=1
XM17[1] vb2 vb2 AVSS AVSS nfet_03v3 L=2u W=2.25u nf=1 ad='int((nf+1)/2) * W/nf * 0.18u' as='int((nf+2)/2) * W/nf * 0.18u'
+ pd='2*int((nf+1)/2) * (W/nf + 0.18u)' ps='2*int((nf+2)/2) * (W/nf + 0.18u)' nrd='0.18u / W' nrs='0.18u / W'
+ sa=0 sb=0 sd=0 m=1
XM17[2] vb2 vb2 AVSS AVSS nfet_03v3 L=2u W=2.25u nf=1 ad='int((nf+1)/2) * W/nf * 0.18u' as='int((nf+2)/2) * W/nf * 0.18u'
+ pd='2*int((nf+1)/2) * (W/nf + 0.18u)' ps='2*int((nf+2)/2) * (W/nf + 0.18u)' nrd='0.18u / W' nrs='0.18u / W'
+ sa=0 sb=0 sd=0 m=1
XM17[3] vb2 vb2 AVSS AVSS nfet_03v3 L=2u W=2.25u nf=1 ad='int((nf+1)/2) * W/nf * 0.18u' as='int((nf+2)/2) * W/nf * 0.18u'
+ pd='2*int((nf+1)/2) * (W/nf + 0.18u)' ps='2*int((nf+2)/2) * (W/nf + 0.18u)' nrd='0.18u / W' nrs='0.18u / W'
+ sa=0 sb=0 sd=0 m=1
XM17[4] vb2 vb2 AVSS AVSS nfet_03v3 L=2u W=2.25u nf=1 ad='int((nf+1)/2) * W/nf * 0.18u' as='int((nf+2)/2) * W/nf * 0.18u'
+ pd='2*int((nf+1)/2) * (W/nf + 0.18u)' ps='2*int((nf+2)/2) * (W/nf + 0.18u)' nrd='0.18u / W' nrs='0.18u / W'
+ sa=0 sb=0 sd=0 m=1
XM12[1] vb4 vb2 AVSS AVSS nfet_03v3 L=2u W=2.25u nf=1 ad='int((nf+1)/2) * W/nf * 0.18u' as='int((nf+2)/2) * W/nf * 0.18u'
+ pd='2*int((nf+1)/2) * (W/nf + 0.18u)' ps='2*int((nf+2)/2) * (W/nf + 0.18u)' nrd='0.18u / W' nrs='0.18u / W'
+ sa=0 sb=0 sd=0 m=1
XM12[2] vb4 vb2 AVSS AVSS nfet_03v3 L=2u W=2.25u nf=1 ad='int((nf+1)/2) * W/nf * 0.18u' as='int((nf+2)/2) * W/nf * 0.18u'
+ pd='2*int((nf+1)/2) * (W/nf + 0.18u)' ps='2*int((nf+2)/2) * (W/nf + 0.18u)' nrd='0.18u / W' nrs='0.18u / W'
+ sa=0 sb=0 sd=0 m=1
XM12[3] vb4 vb2 AVSS AVSS nfet_03v3 L=2u W=2.25u nf=1 ad='int((nf+1)/2) * W/nf * 0.18u' as='int((nf+2)/2) * W/nf * 0.18u'
+ pd='2*int((nf+1)/2) * (W/nf + 0.18u)' ps='2*int((nf+2)/2) * (W/nf + 0.18u)' nrd='0.18u / W' nrs='0.18u / W'
+ sa=0 sb=0 sd=0 m=1
XM12[4] vb4 vb2 AVSS AVSS nfet_03v3 L=2u W=2.25u nf=1 ad='int((nf+1)/2) * W/nf * 0.18u' as='int((nf+2)/2) * W/nf * 0.18u'
+ pd='2*int((nf+1)/2) * (W/nf + 0.18u)' ps='2*int((nf+2)/2) * (W/nf + 0.18u)' nrd='0.18u / W' nrs='0.18u / W'
+ sa=0 sb=0 sd=0 m=1
Vmeas vb1 IREF 0
.save i(vmeas)
Vmeas1 net26 vb3 0
.save i(vmeas1)
V_it1 net28 node_n 0
.save i(v_it1)
V_it2 net27 node_p 0
.save i(v_it2)
x1 M11_S M11_S net27 net28 vi_p vi_n AVDD FC_pfets_x4
V_it3 net29 M11_S 0
.save i(v_it3)
x2 AVDD AVDD net29 net29 vb1 vb1 AVDD FC_pfets_x4
x3 net33 net32 net30 net31 M3_D M3_D AVDD FC_pfets_x4
x4 net30 net31 M3_D vout vb4 vb4 AVDD FC_pfets_x4
V_it4 AVDD net32 0
.save i(v_it4)
V_it5 AVDD net33 0
.save i(v_it5)
x5 node_p node_n M3_D vout vb3 vb3 AVSS FC_nfets
x6 AVSS AVSS net34 net35 vb2 vb2 AVSS FC_nfets_x2
V_it6 node_p net34 0
.save i(v_it6)
V_it7 node_n net35 0
.save i(v_it7)
**.ends

* expanding   symbol:  /home/gmaranhao/Desktop/Bracolin/TIA_Filter/Folded/FC_pfets_x4.sym # of
*+ pins=7
** sym_path: TIA_Filter/Folded/FC_pfets_x4.sym
** sch_path: TIA_Filter/Folded/FC_pfets_x4.sch
.subckt FC_pfets_x4 S1 S2 D1 D2 G1 G2 B
*.iopin S1
*.iopin S2
*.iopin D1
*.iopin D2
*.iopin G1
*.iopin G2
*.iopin B
x1[1] S1 S2 D1 D2 G1 G2 B FC_pfets
x1[2] S1 S2 D1 D2 G1 G2 B FC_pfets
x1[3] S1 S2 D1 D2 G1 G2 B FC_pfets
x1[4] S1 S2 D1 D2 G1 G2 B FC_pfets
.ends


* expanding   symbol:  /home/gmaranhao/Desktop/Bracolin/TIA_Filter/Folded/FC_nfets.sym # of pins=7
** sym_path: TIA_Filter/Folded/FC_nfets.sym
** sch_path: TIA_Filter/Folded/FC_nfets.sch
.subckt FC_nfets S1 S2 D1 D2 G1 G2 B
*.iopin S1
*.iopin S2
*.iopin D1
*.iopin D2
*.iopin G1
*.iopin G2
*.iopin B
XM1[1] D1 G1 S1 B nfet_03v3 L=2u W=2u nf=1 ad='int((nf+1)/2) * W/nf * 0.18u' as='int((nf+2)/2) * W/nf * 0.18u'
+ pd='2*int((nf+1)/2) * (W/nf + 0.18u)' ps='2*int((nf+2)/2) * (W/nf + 0.18u)' nrd='0.18u / W' nrs='0.18u / W'
+ sa=0 sb=0 sd=0 m=1
XM1[2] D1 G1 S1 B nfet_03v3 L=2u W=2u nf=1 ad='int((nf+1)/2) * W/nf * 0.18u' as='int((nf+2)/2) * W/nf * 0.18u'
+ pd='2*int((nf+1)/2) * (W/nf + 0.18u)' ps='2*int((nf+2)/2) * (W/nf + 0.18u)' nrd='0.18u / W' nrs='0.18u / W'
+ sa=0 sb=0 sd=0 m=1
XM1[3] D1 G1 S1 B nfet_03v3 L=2u W=2u nf=1 ad='int((nf+1)/2) * W/nf * 0.18u' as='int((nf+2)/2) * W/nf * 0.18u'
+ pd='2*int((nf+1)/2) * (W/nf + 0.18u)' ps='2*int((nf+2)/2) * (W/nf + 0.18u)' nrd='0.18u / W' nrs='0.18u / W'
+ sa=0 sb=0 sd=0 m=1
XM1[4] D1 G1 S1 B nfet_03v3 L=2u W=2u nf=1 ad='int((nf+1)/2) * W/nf * 0.18u' as='int((nf+2)/2) * W/nf * 0.18u'
+ pd='2*int((nf+1)/2) * (W/nf + 0.18u)' ps='2*int((nf+2)/2) * (W/nf + 0.18u)' nrd='0.18u / W' nrs='0.18u / W'
+ sa=0 sb=0 sd=0 m=1
XM1[5] D1 G1 S1 B nfet_03v3 L=2u W=2u nf=1 ad='int((nf+1)/2) * W/nf * 0.18u' as='int((nf+2)/2) * W/nf * 0.18u'
+ pd='2*int((nf+1)/2) * (W/nf + 0.18u)' ps='2*int((nf+2)/2) * (W/nf + 0.18u)' nrd='0.18u / W' nrs='0.18u / W'
+ sa=0 sb=0 sd=0 m=1
XM1[6] D1 G1 S1 B nfet_03v3 L=2u W=2u nf=1 ad='int((nf+1)/2) * W/nf * 0.18u' as='int((nf+2)/2) * W/nf * 0.18u'
+ pd='2*int((nf+1)/2) * (W/nf + 0.18u)' ps='2*int((nf+2)/2) * (W/nf + 0.18u)' nrd='0.18u / W' nrs='0.18u / W'
+ sa=0 sb=0 sd=0 m=1
XM1[7] D1 G1 S1 B nfet_03v3 L=2u W=2u nf=1 ad='int((nf+1)/2) * W/nf * 0.18u' as='int((nf+2)/2) * W/nf * 0.18u'
+ pd='2*int((nf+1)/2) * (W/nf + 0.18u)' ps='2*int((nf+2)/2) * (W/nf + 0.18u)' nrd='0.18u / W' nrs='0.18u / W'
+ sa=0 sb=0 sd=0 m=1
XM1[8] D1 G1 S1 B nfet_03v3 L=2u W=2u nf=1 ad='int((nf+1)/2) * W/nf * 0.18u' as='int((nf+2)/2) * W/nf * 0.18u'
+ pd='2*int((nf+1)/2) * (W/nf + 0.18u)' ps='2*int((nf+2)/2) * (W/nf + 0.18u)' nrd='0.18u / W' nrs='0.18u / W'
+ sa=0 sb=0 sd=0 m=1
XM1[9] D1 G1 S1 B nfet_03v3 L=2u W=2u nf=1 ad='int((nf+1)/2) * W/nf * 0.18u' as='int((nf+2)/2) * W/nf * 0.18u'
+ pd='2*int((nf+1)/2) * (W/nf + 0.18u)' ps='2*int((nf+2)/2) * (W/nf + 0.18u)' nrd='0.18u / W' nrs='0.18u / W'
+ sa=0 sb=0 sd=0 m=1
XM1[10] D1 G1 S1 B nfet_03v3 L=2u W=2u nf=1 ad='int((nf+1)/2) * W/nf * 0.18u' as='int((nf+2)/2) * W/nf * 0.18u'
+ pd='2*int((nf+1)/2) * (W/nf + 0.18u)' ps='2*int((nf+2)/2) * (W/nf + 0.18u)' nrd='0.18u / W' nrs='0.18u / W'
+ sa=0 sb=0 sd=0 m=1
XM1[11] D1 G1 S1 B nfet_03v3 L=2u W=2u nf=1 ad='int((nf+1)/2) * W/nf * 0.18u' as='int((nf+2)/2) * W/nf * 0.18u'
+ pd='2*int((nf+1)/2) * (W/nf + 0.18u)' ps='2*int((nf+2)/2) * (W/nf + 0.18u)' nrd='0.18u / W' nrs='0.18u / W'
+ sa=0 sb=0 sd=0 m=1
XM1[12] D1 G1 S1 B nfet_03v3 L=2u W=2u nf=1 ad='int((nf+1)/2) * W/nf * 0.18u' as='int((nf+2)/2) * W/nf * 0.18u'
+ pd='2*int((nf+1)/2) * (W/nf + 0.18u)' ps='2*int((nf+2)/2) * (W/nf + 0.18u)' nrd='0.18u / W' nrs='0.18u / W'
+ sa=0 sb=0 sd=0 m=1
XM1[13] D1 G1 S1 B nfet_03v3 L=2u W=2u nf=1 ad='int((nf+1)/2) * W/nf * 0.18u' as='int((nf+2)/2) * W/nf * 0.18u'
+ pd='2*int((nf+1)/2) * (W/nf + 0.18u)' ps='2*int((nf+2)/2) * (W/nf + 0.18u)' nrd='0.18u / W' nrs='0.18u / W'
+ sa=0 sb=0 sd=0 m=1
XM1[14] D1 G1 S1 B nfet_03v3 L=2u W=2u nf=1 ad='int((nf+1)/2) * W/nf * 0.18u' as='int((nf+2)/2) * W/nf * 0.18u'
+ pd='2*int((nf+1)/2) * (W/nf + 0.18u)' ps='2*int((nf+2)/2) * (W/nf + 0.18u)' nrd='0.18u / W' nrs='0.18u / W'
+ sa=0 sb=0 sd=0 m=1
XM1[15] D1 G1 S1 B nfet_03v3 L=2u W=2u nf=1 ad='int((nf+1)/2) * W/nf * 0.18u' as='int((nf+2)/2) * W/nf * 0.18u'
+ pd='2*int((nf+1)/2) * (W/nf + 0.18u)' ps='2*int((nf+2)/2) * (W/nf + 0.18u)' nrd='0.18u / W' nrs='0.18u / W'
+ sa=0 sb=0 sd=0 m=1
XM1[16] D1 G1 S1 B nfet_03v3 L=2u W=2u nf=1 ad='int((nf+1)/2) * W/nf * 0.18u' as='int((nf+2)/2) * W/nf * 0.18u'
+ pd='2*int((nf+1)/2) * (W/nf + 0.18u)' ps='2*int((nf+2)/2) * (W/nf + 0.18u)' nrd='0.18u / W' nrs='0.18u / W'
+ sa=0 sb=0 sd=0 m=1
XM1[17] D1 G1 S1 B nfet_03v3 L=2u W=2u nf=1 ad='int((nf+1)/2) * W/nf * 0.18u' as='int((nf+2)/2) * W/nf * 0.18u'
+ pd='2*int((nf+1)/2) * (W/nf + 0.18u)' ps='2*int((nf+2)/2) * (W/nf + 0.18u)' nrd='0.18u / W' nrs='0.18u / W'
+ sa=0 sb=0 sd=0 m=1
XM1[18] D1 G1 S1 B nfet_03v3 L=2u W=2u nf=1 ad='int((nf+1)/2) * W/nf * 0.18u' as='int((nf+2)/2) * W/nf * 0.18u'
+ pd='2*int((nf+1)/2) * (W/nf + 0.18u)' ps='2*int((nf+2)/2) * (W/nf + 0.18u)' nrd='0.18u / W' nrs='0.18u / W'
+ sa=0 sb=0 sd=0 m=1
XM2[1] D2 G2 S2 B nfet_03v3 L=2u W=2u nf=1 ad='int((nf+1)/2) * W/nf * 0.18u' as='int((nf+2)/2) * W/nf * 0.18u'
+ pd='2*int((nf+1)/2) * (W/nf + 0.18u)' ps='2*int((nf+2)/2) * (W/nf + 0.18u)' nrd='0.18u / W' nrs='0.18u / W'
+ sa=0 sb=0 sd=0 m=1
XM2[2] D2 G2 S2 B nfet_03v3 L=2u W=2u nf=1 ad='int((nf+1)/2) * W/nf * 0.18u' as='int((nf+2)/2) * W/nf * 0.18u'
+ pd='2*int((nf+1)/2) * (W/nf + 0.18u)' ps='2*int((nf+2)/2) * (W/nf + 0.18u)' nrd='0.18u / W' nrs='0.18u / W'
+ sa=0 sb=0 sd=0 m=1
XM2[3] D2 G2 S2 B nfet_03v3 L=2u W=2u nf=1 ad='int((nf+1)/2) * W/nf * 0.18u' as='int((nf+2)/2) * W/nf * 0.18u'
+ pd='2*int((nf+1)/2) * (W/nf + 0.18u)' ps='2*int((nf+2)/2) * (W/nf + 0.18u)' nrd='0.18u / W' nrs='0.18u / W'
+ sa=0 sb=0 sd=0 m=1
XM2[4] D2 G2 S2 B nfet_03v3 L=2u W=2u nf=1 ad='int((nf+1)/2) * W/nf * 0.18u' as='int((nf+2)/2) * W/nf * 0.18u'
+ pd='2*int((nf+1)/2) * (W/nf + 0.18u)' ps='2*int((nf+2)/2) * (W/nf + 0.18u)' nrd='0.18u / W' nrs='0.18u / W'
+ sa=0 sb=0 sd=0 m=1
XM2[5] D2 G2 S2 B nfet_03v3 L=2u W=2u nf=1 ad='int((nf+1)/2) * W/nf * 0.18u' as='int((nf+2)/2) * W/nf * 0.18u'
+ pd='2*int((nf+1)/2) * (W/nf + 0.18u)' ps='2*int((nf+2)/2) * (W/nf + 0.18u)' nrd='0.18u / W' nrs='0.18u / W'
+ sa=0 sb=0 sd=0 m=1
XM2[6] D2 G2 S2 B nfet_03v3 L=2u W=2u nf=1 ad='int((nf+1)/2) * W/nf * 0.18u' as='int((nf+2)/2) * W/nf * 0.18u'
+ pd='2*int((nf+1)/2) * (W/nf + 0.18u)' ps='2*int((nf+2)/2) * (W/nf + 0.18u)' nrd='0.18u / W' nrs='0.18u / W'
+ sa=0 sb=0 sd=0 m=1
XM2[7] D2 G2 S2 B nfet_03v3 L=2u W=2u nf=1 ad='int((nf+1)/2) * W/nf * 0.18u' as='int((nf+2)/2) * W/nf * 0.18u'
+ pd='2*int((nf+1)/2) * (W/nf + 0.18u)' ps='2*int((nf+2)/2) * (W/nf + 0.18u)' nrd='0.18u / W' nrs='0.18u / W'
+ sa=0 sb=0 sd=0 m=1
XM2[8] D2 G2 S2 B nfet_03v3 L=2u W=2u nf=1 ad='int((nf+1)/2) * W/nf * 0.18u' as='int((nf+2)/2) * W/nf * 0.18u'
+ pd='2*int((nf+1)/2) * (W/nf + 0.18u)' ps='2*int((nf+2)/2) * (W/nf + 0.18u)' nrd='0.18u / W' nrs='0.18u / W'
+ sa=0 sb=0 sd=0 m=1
XM2[9] D2 G2 S2 B nfet_03v3 L=2u W=2u nf=1 ad='int((nf+1)/2) * W/nf * 0.18u' as='int((nf+2)/2) * W/nf * 0.18u'
+ pd='2*int((nf+1)/2) * (W/nf + 0.18u)' ps='2*int((nf+2)/2) * (W/nf + 0.18u)' nrd='0.18u / W' nrs='0.18u / W'
+ sa=0 sb=0 sd=0 m=1
XM2[10] D2 G2 S2 B nfet_03v3 L=2u W=2u nf=1 ad='int((nf+1)/2) * W/nf * 0.18u' as='int((nf+2)/2) * W/nf * 0.18u'
+ pd='2*int((nf+1)/2) * (W/nf + 0.18u)' ps='2*int((nf+2)/2) * (W/nf + 0.18u)' nrd='0.18u / W' nrs='0.18u / W'
+ sa=0 sb=0 sd=0 m=1
XM2[11] D2 G2 S2 B nfet_03v3 L=2u W=2u nf=1 ad='int((nf+1)/2) * W/nf * 0.18u' as='int((nf+2)/2) * W/nf * 0.18u'
+ pd='2*int((nf+1)/2) * (W/nf + 0.18u)' ps='2*int((nf+2)/2) * (W/nf + 0.18u)' nrd='0.18u / W' nrs='0.18u / W'
+ sa=0 sb=0 sd=0 m=1
XM2[12] D2 G2 S2 B nfet_03v3 L=2u W=2u nf=1 ad='int((nf+1)/2) * W/nf * 0.18u' as='int((nf+2)/2) * W/nf * 0.18u'
+ pd='2*int((nf+1)/2) * (W/nf + 0.18u)' ps='2*int((nf+2)/2) * (W/nf + 0.18u)' nrd='0.18u / W' nrs='0.18u / W'
+ sa=0 sb=0 sd=0 m=1
XM2[13] D2 G2 S2 B nfet_03v3 L=2u W=2u nf=1 ad='int((nf+1)/2) * W/nf * 0.18u' as='int((nf+2)/2) * W/nf * 0.18u'
+ pd='2*int((nf+1)/2) * (W/nf + 0.18u)' ps='2*int((nf+2)/2) * (W/nf + 0.18u)' nrd='0.18u / W' nrs='0.18u / W'
+ sa=0 sb=0 sd=0 m=1
XM2[14] D2 G2 S2 B nfet_03v3 L=2u W=2u nf=1 ad='int((nf+1)/2) * W/nf * 0.18u' as='int((nf+2)/2) * W/nf * 0.18u'
+ pd='2*int((nf+1)/2) * (W/nf + 0.18u)' ps='2*int((nf+2)/2) * (W/nf + 0.18u)' nrd='0.18u / W' nrs='0.18u / W'
+ sa=0 sb=0 sd=0 m=1
XM2[15] D2 G2 S2 B nfet_03v3 L=2u W=2u nf=1 ad='int((nf+1)/2) * W/nf * 0.18u' as='int((nf+2)/2) * W/nf * 0.18u'
+ pd='2*int((nf+1)/2) * (W/nf + 0.18u)' ps='2*int((nf+2)/2) * (W/nf + 0.18u)' nrd='0.18u / W' nrs='0.18u / W'
+ sa=0 sb=0 sd=0 m=1
XM2[16] D2 G2 S2 B nfet_03v3 L=2u W=2u nf=1 ad='int((nf+1)/2) * W/nf * 0.18u' as='int((nf+2)/2) * W/nf * 0.18u'
+ pd='2*int((nf+1)/2) * (W/nf + 0.18u)' ps='2*int((nf+2)/2) * (W/nf + 0.18u)' nrd='0.18u / W' nrs='0.18u / W'
+ sa=0 sb=0 sd=0 m=1
XM2[17] D2 G2 S2 B nfet_03v3 L=2u W=2u nf=1 ad='int((nf+1)/2) * W/nf * 0.18u' as='int((nf+2)/2) * W/nf * 0.18u'
+ pd='2*int((nf+1)/2) * (W/nf + 0.18u)' ps='2*int((nf+2)/2) * (W/nf + 0.18u)' nrd='0.18u / W' nrs='0.18u / W'
+ sa=0 sb=0 sd=0 m=1
XM2[18] D2 G2 S2 B nfet_03v3 L=2u W=2u nf=1 ad='int((nf+1)/2) * W/nf * 0.18u' as='int((nf+2)/2) * W/nf * 0.18u'
+ pd='2*int((nf+1)/2) * (W/nf + 0.18u)' ps='2*int((nf+2)/2) * (W/nf + 0.18u)' nrd='0.18u / W' nrs='0.18u / W'
+ sa=0 sb=0 sd=0 m=1
.ends


* expanding   symbol:  /home/gmaranhao/Desktop/Bracolin/TIA_Filter/Folded/FC_nfets_x2.sym # of
*+ pins=7
** sym_path: Voltage_Reference/LDO/Folded/FC_nfets_x2.sym
** sch_path: Voltage_Reference/LDO/Folded/FC_nfets_x2.sch
.subckt FC_nfets_x2 S1 S2 D1 D2 G1 G2 B
*.iopin S1
*.iopin S2
*.iopin D1
*.iopin D2
*.iopin G1
*.iopin G2
*.iopin B
x1[1] S1 S2 D1 D2 G1 G2 B FC_nfets
x1[2] S1 S2 D1 D2 G1 G2 B FC_nfets
.ends


* expanding   symbol:  /home/gmaranhao/Desktop/Bracolin/TIA_Filter/Folded/FC_pfets.sym # of pins=7
** sym_path: TIA_Filter/Folded/FC_pfets.sym
** sch_path: TIA_Filter/Folded/FC_pfets.sch
.subckt FC_pfets S1 S2 D1 D2 G1 G2 B
*.iopin S1
*.iopin S2
*.iopin D1
*.iopin D2
*.iopin G1
*.iopin G2
*.iopin B
XM1[1] D1 G1 S1 B pfet_03v3 L=2u W=2u nf=1 ad='int((nf+1)/2) * W/nf * 0.18u' as='int((nf+2)/2) * W/nf * 0.18u'
+ pd='2*int((nf+1)/2) * (W/nf + 0.18u)' ps='2*int((nf+2)/2) * (W/nf + 0.18u)' nrd='0.18u / W' nrs='0.18u / W'
+ sa=0 sb=0 sd=0 m=1
XM1[2] D1 G1 S1 B pfet_03v3 L=2u W=2u nf=1 ad='int((nf+1)/2) * W/nf * 0.18u' as='int((nf+2)/2) * W/nf * 0.18u'
+ pd='2*int((nf+1)/2) * (W/nf + 0.18u)' ps='2*int((nf+2)/2) * (W/nf + 0.18u)' nrd='0.18u / W' nrs='0.18u / W'
+ sa=0 sb=0 sd=0 m=1
XM1[3] D1 G1 S1 B pfet_03v3 L=2u W=2u nf=1 ad='int((nf+1)/2) * W/nf * 0.18u' as='int((nf+2)/2) * W/nf * 0.18u'
+ pd='2*int((nf+1)/2) * (W/nf + 0.18u)' ps='2*int((nf+2)/2) * (W/nf + 0.18u)' nrd='0.18u / W' nrs='0.18u / W'
+ sa=0 sb=0 sd=0 m=1
XM1[4] D1 G1 S1 B pfet_03v3 L=2u W=2u nf=1 ad='int((nf+1)/2) * W/nf * 0.18u' as='int((nf+2)/2) * W/nf * 0.18u'
+ pd='2*int((nf+1)/2) * (W/nf + 0.18u)' ps='2*int((nf+2)/2) * (W/nf + 0.18u)' nrd='0.18u / W' nrs='0.18u / W'
+ sa=0 sb=0 sd=0 m=1
XM1[5] D1 G1 S1 B pfet_03v3 L=2u W=2u nf=1 ad='int((nf+1)/2) * W/nf * 0.18u' as='int((nf+2)/2) * W/nf * 0.18u'
+ pd='2*int((nf+1)/2) * (W/nf + 0.18u)' ps='2*int((nf+2)/2) * (W/nf + 0.18u)' nrd='0.18u / W' nrs='0.18u / W'
+ sa=0 sb=0 sd=0 m=1
XM1[6] D1 G1 S1 B pfet_03v3 L=2u W=2u nf=1 ad='int((nf+1)/2) * W/nf * 0.18u' as='int((nf+2)/2) * W/nf * 0.18u'
+ pd='2*int((nf+1)/2) * (W/nf + 0.18u)' ps='2*int((nf+2)/2) * (W/nf + 0.18u)' nrd='0.18u / W' nrs='0.18u / W'
+ sa=0 sb=0 sd=0 m=1
XM1[7] D1 G1 S1 B pfet_03v3 L=2u W=2u nf=1 ad='int((nf+1)/2) * W/nf * 0.18u' as='int((nf+2)/2) * W/nf * 0.18u'
+ pd='2*int((nf+1)/2) * (W/nf + 0.18u)' ps='2*int((nf+2)/2) * (W/nf + 0.18u)' nrd='0.18u / W' nrs='0.18u / W'
+ sa=0 sb=0 sd=0 m=1
XM1[8] D1 G1 S1 B pfet_03v3 L=2u W=2u nf=1 ad='int((nf+1)/2) * W/nf * 0.18u' as='int((nf+2)/2) * W/nf * 0.18u'
+ pd='2*int((nf+1)/2) * (W/nf + 0.18u)' ps='2*int((nf+2)/2) * (W/nf + 0.18u)' nrd='0.18u / W' nrs='0.18u / W'
+ sa=0 sb=0 sd=0 m=1
XM1[9] D1 G1 S1 B pfet_03v3 L=2u W=2u nf=1 ad='int((nf+1)/2) * W/nf * 0.18u' as='int((nf+2)/2) * W/nf * 0.18u'
+ pd='2*int((nf+1)/2) * (W/nf + 0.18u)' ps='2*int((nf+2)/2) * (W/nf + 0.18u)' nrd='0.18u / W' nrs='0.18u / W'
+ sa=0 sb=0 sd=0 m=1
XM1[10] D1 G1 S1 B pfet_03v3 L=2u W=2u nf=1 ad='int((nf+1)/2) * W/nf * 0.18u' as='int((nf+2)/2) * W/nf * 0.18u'
+ pd='2*int((nf+1)/2) * (W/nf + 0.18u)' ps='2*int((nf+2)/2) * (W/nf + 0.18u)' nrd='0.18u / W' nrs='0.18u / W'
+ sa=0 sb=0 sd=0 m=1
XM1[11] D1 G1 S1 B pfet_03v3 L=2u W=2u nf=1 ad='int((nf+1)/2) * W/nf * 0.18u' as='int((nf+2)/2) * W/nf * 0.18u'
+ pd='2*int((nf+1)/2) * (W/nf + 0.18u)' ps='2*int((nf+2)/2) * (W/nf + 0.18u)' nrd='0.18u / W' nrs='0.18u / W'
+ sa=0 sb=0 sd=0 m=1
XM1[12] D1 G1 S1 B pfet_03v3 L=2u W=2u nf=1 ad='int((nf+1)/2) * W/nf * 0.18u' as='int((nf+2)/2) * W/nf * 0.18u'
+ pd='2*int((nf+1)/2) * (W/nf + 0.18u)' ps='2*int((nf+2)/2) * (W/nf + 0.18u)' nrd='0.18u / W' nrs='0.18u / W'
+ sa=0 sb=0 sd=0 m=1
XM1[13] D1 G1 S1 B pfet_03v3 L=2u W=2u nf=1 ad='int((nf+1)/2) * W/nf * 0.18u' as='int((nf+2)/2) * W/nf * 0.18u'
+ pd='2*int((nf+1)/2) * (W/nf + 0.18u)' ps='2*int((nf+2)/2) * (W/nf + 0.18u)' nrd='0.18u / W' nrs='0.18u / W'
+ sa=0 sb=0 sd=0 m=1
XM1[14] D1 G1 S1 B pfet_03v3 L=2u W=2u nf=1 ad='int((nf+1)/2) * W/nf * 0.18u' as='int((nf+2)/2) * W/nf * 0.18u'
+ pd='2*int((nf+1)/2) * (W/nf + 0.18u)' ps='2*int((nf+2)/2) * (W/nf + 0.18u)' nrd='0.18u / W' nrs='0.18u / W'
+ sa=0 sb=0 sd=0 m=1
XM1[15] D1 G1 S1 B pfet_03v3 L=2u W=2u nf=1 ad='int((nf+1)/2) * W/nf * 0.18u' as='int((nf+2)/2) * W/nf * 0.18u'
+ pd='2*int((nf+1)/2) * (W/nf + 0.18u)' ps='2*int((nf+2)/2) * (W/nf + 0.18u)' nrd='0.18u / W' nrs='0.18u / W'
+ sa=0 sb=0 sd=0 m=1
XM1[16] D1 G1 S1 B pfet_03v3 L=2u W=2u nf=1 ad='int((nf+1)/2) * W/nf * 0.18u' as='int((nf+2)/2) * W/nf * 0.18u'
+ pd='2*int((nf+1)/2) * (W/nf + 0.18u)' ps='2*int((nf+2)/2) * (W/nf + 0.18u)' nrd='0.18u / W' nrs='0.18u / W'
+ sa=0 sb=0 sd=0 m=1
XM1[17] D1 G1 S1 B pfet_03v3 L=2u W=2u nf=1 ad='int((nf+1)/2) * W/nf * 0.18u' as='int((nf+2)/2) * W/nf * 0.18u'
+ pd='2*int((nf+1)/2) * (W/nf + 0.18u)' ps='2*int((nf+2)/2) * (W/nf + 0.18u)' nrd='0.18u / W' nrs='0.18u / W'
+ sa=0 sb=0 sd=0 m=1
XM1[18] D1 G1 S1 B pfet_03v3 L=2u W=2u nf=1 ad='int((nf+1)/2) * W/nf * 0.18u' as='int((nf+2)/2) * W/nf * 0.18u'
+ pd='2*int((nf+1)/2) * (W/nf + 0.18u)' ps='2*int((nf+2)/2) * (W/nf + 0.18u)' nrd='0.18u / W' nrs='0.18u / W'
+ sa=0 sb=0 sd=0 m=1
XM1[19] D1 G1 S1 B pfet_03v3 L=2u W=2u nf=1 ad='int((nf+1)/2) * W/nf * 0.18u' as='int((nf+2)/2) * W/nf * 0.18u'
+ pd='2*int((nf+1)/2) * (W/nf + 0.18u)' ps='2*int((nf+2)/2) * (W/nf + 0.18u)' nrd='0.18u / W' nrs='0.18u / W'
+ sa=0 sb=0 sd=0 m=1
XM1[20] D1 G1 S1 B pfet_03v3 L=2u W=2u nf=1 ad='int((nf+1)/2) * W/nf * 0.18u' as='int((nf+2)/2) * W/nf * 0.18u'
+ pd='2*int((nf+1)/2) * (W/nf + 0.18u)' ps='2*int((nf+2)/2) * (W/nf + 0.18u)' nrd='0.18u / W' nrs='0.18u / W'
+ sa=0 sb=0 sd=0 m=1
XM1[21] D1 G1 S1 B pfet_03v3 L=2u W=2u nf=1 ad='int((nf+1)/2) * W/nf * 0.18u' as='int((nf+2)/2) * W/nf * 0.18u'
+ pd='2*int((nf+1)/2) * (W/nf + 0.18u)' ps='2*int((nf+2)/2) * (W/nf + 0.18u)' nrd='0.18u / W' nrs='0.18u / W'
+ sa=0 sb=0 sd=0 m=1
XM1[22] D1 G1 S1 B pfet_03v3 L=2u W=2u nf=1 ad='int((nf+1)/2) * W/nf * 0.18u' as='int((nf+2)/2) * W/nf * 0.18u'
+ pd='2*int((nf+1)/2) * (W/nf + 0.18u)' ps='2*int((nf+2)/2) * (W/nf + 0.18u)' nrd='0.18u / W' nrs='0.18u / W'
+ sa=0 sb=0 sd=0 m=1
XM2[1] D2 G2 S2 B pfet_03v3 L=2u W=2u nf=1 ad='int((nf+1)/2) * W/nf * 0.18u' as='int((nf+2)/2) * W/nf * 0.18u'
+ pd='2*int((nf+1)/2) * (W/nf + 0.18u)' ps='2*int((nf+2)/2) * (W/nf + 0.18u)' nrd='0.18u / W' nrs='0.18u / W'
+ sa=0 sb=0 sd=0 m=1
XM2[2] D2 G2 S2 B pfet_03v3 L=2u W=2u nf=1 ad='int((nf+1)/2) * W/nf * 0.18u' as='int((nf+2)/2) * W/nf * 0.18u'
+ pd='2*int((nf+1)/2) * (W/nf + 0.18u)' ps='2*int((nf+2)/2) * (W/nf + 0.18u)' nrd='0.18u / W' nrs='0.18u / W'
+ sa=0 sb=0 sd=0 m=1
XM2[3] D2 G2 S2 B pfet_03v3 L=2u W=2u nf=1 ad='int((nf+1)/2) * W/nf * 0.18u' as='int((nf+2)/2) * W/nf * 0.18u'
+ pd='2*int((nf+1)/2) * (W/nf + 0.18u)' ps='2*int((nf+2)/2) * (W/nf + 0.18u)' nrd='0.18u / W' nrs='0.18u / W'
+ sa=0 sb=0 sd=0 m=1
XM2[4] D2 G2 S2 B pfet_03v3 L=2u W=2u nf=1 ad='int((nf+1)/2) * W/nf * 0.18u' as='int((nf+2)/2) * W/nf * 0.18u'
+ pd='2*int((nf+1)/2) * (W/nf + 0.18u)' ps='2*int((nf+2)/2) * (W/nf + 0.18u)' nrd='0.18u / W' nrs='0.18u / W'
+ sa=0 sb=0 sd=0 m=1
XM2[5] D2 G2 S2 B pfet_03v3 L=2u W=2u nf=1 ad='int((nf+1)/2) * W/nf * 0.18u' as='int((nf+2)/2) * W/nf * 0.18u'
+ pd='2*int((nf+1)/2) * (W/nf + 0.18u)' ps='2*int((nf+2)/2) * (W/nf + 0.18u)' nrd='0.18u / W' nrs='0.18u / W'
+ sa=0 sb=0 sd=0 m=1
XM2[6] D2 G2 S2 B pfet_03v3 L=2u W=2u nf=1 ad='int((nf+1)/2) * W/nf * 0.18u' as='int((nf+2)/2) * W/nf * 0.18u'
+ pd='2*int((nf+1)/2) * (W/nf + 0.18u)' ps='2*int((nf+2)/2) * (W/nf + 0.18u)' nrd='0.18u / W' nrs='0.18u / W'
+ sa=0 sb=0 sd=0 m=1
XM2[7] D2 G2 S2 B pfet_03v3 L=2u W=2u nf=1 ad='int((nf+1)/2) * W/nf * 0.18u' as='int((nf+2)/2) * W/nf * 0.18u'
+ pd='2*int((nf+1)/2) * (W/nf + 0.18u)' ps='2*int((nf+2)/2) * (W/nf + 0.18u)' nrd='0.18u / W' nrs='0.18u / W'
+ sa=0 sb=0 sd=0 m=1
XM2[8] D2 G2 S2 B pfet_03v3 L=2u W=2u nf=1 ad='int((nf+1)/2) * W/nf * 0.18u' as='int((nf+2)/2) * W/nf * 0.18u'
+ pd='2*int((nf+1)/2) * (W/nf + 0.18u)' ps='2*int((nf+2)/2) * (W/nf + 0.18u)' nrd='0.18u / W' nrs='0.18u / W'
+ sa=0 sb=0 sd=0 m=1
XM2[9] D2 G2 S2 B pfet_03v3 L=2u W=2u nf=1 ad='int((nf+1)/2) * W/nf * 0.18u' as='int((nf+2)/2) * W/nf * 0.18u'
+ pd='2*int((nf+1)/2) * (W/nf + 0.18u)' ps='2*int((nf+2)/2) * (W/nf + 0.18u)' nrd='0.18u / W' nrs='0.18u / W'
+ sa=0 sb=0 sd=0 m=1
XM2[10] D2 G2 S2 B pfet_03v3 L=2u W=2u nf=1 ad='int((nf+1)/2) * W/nf * 0.18u' as='int((nf+2)/2) * W/nf * 0.18u'
+ pd='2*int((nf+1)/2) * (W/nf + 0.18u)' ps='2*int((nf+2)/2) * (W/nf + 0.18u)' nrd='0.18u / W' nrs='0.18u / W'
+ sa=0 sb=0 sd=0 m=1
XM2[11] D2 G2 S2 B pfet_03v3 L=2u W=2u nf=1 ad='int((nf+1)/2) * W/nf * 0.18u' as='int((nf+2)/2) * W/nf * 0.18u'
+ pd='2*int((nf+1)/2) * (W/nf + 0.18u)' ps='2*int((nf+2)/2) * (W/nf + 0.18u)' nrd='0.18u / W' nrs='0.18u / W'
+ sa=0 sb=0 sd=0 m=1
XM2[12] D2 G2 S2 B pfet_03v3 L=2u W=2u nf=1 ad='int((nf+1)/2) * W/nf * 0.18u' as='int((nf+2)/2) * W/nf * 0.18u'
+ pd='2*int((nf+1)/2) * (W/nf + 0.18u)' ps='2*int((nf+2)/2) * (W/nf + 0.18u)' nrd='0.18u / W' nrs='0.18u / W'
+ sa=0 sb=0 sd=0 m=1
XM2[13] D2 G2 S2 B pfet_03v3 L=2u W=2u nf=1 ad='int((nf+1)/2) * W/nf * 0.18u' as='int((nf+2)/2) * W/nf * 0.18u'
+ pd='2*int((nf+1)/2) * (W/nf + 0.18u)' ps='2*int((nf+2)/2) * (W/nf + 0.18u)' nrd='0.18u / W' nrs='0.18u / W'
+ sa=0 sb=0 sd=0 m=1
XM2[14] D2 G2 S2 B pfet_03v3 L=2u W=2u nf=1 ad='int((nf+1)/2) * W/nf * 0.18u' as='int((nf+2)/2) * W/nf * 0.18u'
+ pd='2*int((nf+1)/2) * (W/nf + 0.18u)' ps='2*int((nf+2)/2) * (W/nf + 0.18u)' nrd='0.18u / W' nrs='0.18u / W'
+ sa=0 sb=0 sd=0 m=1
XM2[15] D2 G2 S2 B pfet_03v3 L=2u W=2u nf=1 ad='int((nf+1)/2) * W/nf * 0.18u' as='int((nf+2)/2) * W/nf * 0.18u'
+ pd='2*int((nf+1)/2) * (W/nf + 0.18u)' ps='2*int((nf+2)/2) * (W/nf + 0.18u)' nrd='0.18u / W' nrs='0.18u / W'
+ sa=0 sb=0 sd=0 m=1
XM2[16] D2 G2 S2 B pfet_03v3 L=2u W=2u nf=1 ad='int((nf+1)/2) * W/nf * 0.18u' as='int((nf+2)/2) * W/nf * 0.18u'
+ pd='2*int((nf+1)/2) * (W/nf + 0.18u)' ps='2*int((nf+2)/2) * (W/nf + 0.18u)' nrd='0.18u / W' nrs='0.18u / W'
+ sa=0 sb=0 sd=0 m=1
XM2[17] D2 G2 S2 B pfet_03v3 L=2u W=2u nf=1 ad='int((nf+1)/2) * W/nf * 0.18u' as='int((nf+2)/2) * W/nf * 0.18u'
+ pd='2*int((nf+1)/2) * (W/nf + 0.18u)' ps='2*int((nf+2)/2) * (W/nf + 0.18u)' nrd='0.18u / W' nrs='0.18u / W'
+ sa=0 sb=0 sd=0 m=1
XM2[18] D2 G2 S2 B pfet_03v3 L=2u W=2u nf=1 ad='int((nf+1)/2) * W/nf * 0.18u' as='int((nf+2)/2) * W/nf * 0.18u'
+ pd='2*int((nf+1)/2) * (W/nf + 0.18u)' ps='2*int((nf+2)/2) * (W/nf + 0.18u)' nrd='0.18u / W' nrs='0.18u / W'
+ sa=0 sb=0 sd=0 m=1
XM2[19] D2 G2 S2 B pfet_03v3 L=2u W=2u nf=1 ad='int((nf+1)/2) * W/nf * 0.18u' as='int((nf+2)/2) * W/nf * 0.18u'
+ pd='2*int((nf+1)/2) * (W/nf + 0.18u)' ps='2*int((nf+2)/2) * (W/nf + 0.18u)' nrd='0.18u / W' nrs='0.18u / W'
+ sa=0 sb=0 sd=0 m=1
XM2[20] D2 G2 S2 B pfet_03v3 L=2u W=2u nf=1 ad='int((nf+1)/2) * W/nf * 0.18u' as='int((nf+2)/2) * W/nf * 0.18u'
+ pd='2*int((nf+1)/2) * (W/nf + 0.18u)' ps='2*int((nf+2)/2) * (W/nf + 0.18u)' nrd='0.18u / W' nrs='0.18u / W'
+ sa=0 sb=0 sd=0 m=1
XM2[21] D2 G2 S2 B pfet_03v3 L=2u W=2u nf=1 ad='int((nf+1)/2) * W/nf * 0.18u' as='int((nf+2)/2) * W/nf * 0.18u'
+ pd='2*int((nf+1)/2) * (W/nf + 0.18u)' ps='2*int((nf+2)/2) * (W/nf + 0.18u)' nrd='0.18u / W' nrs='0.18u / W'
+ sa=0 sb=0 sd=0 m=1
XM2[22] D2 G2 S2 B pfet_03v3 L=2u W=2u nf=1 ad='int((nf+1)/2) * W/nf * 0.18u' as='int((nf+2)/2) * W/nf * 0.18u'
+ pd='2*int((nf+1)/2) * (W/nf + 0.18u)' ps='2*int((nf+2)/2) * (W/nf + 0.18u)' nrd='0.18u / W' nrs='0.18u / W'
+ sa=0 sb=0 sd=0 m=1
.ends

.end
